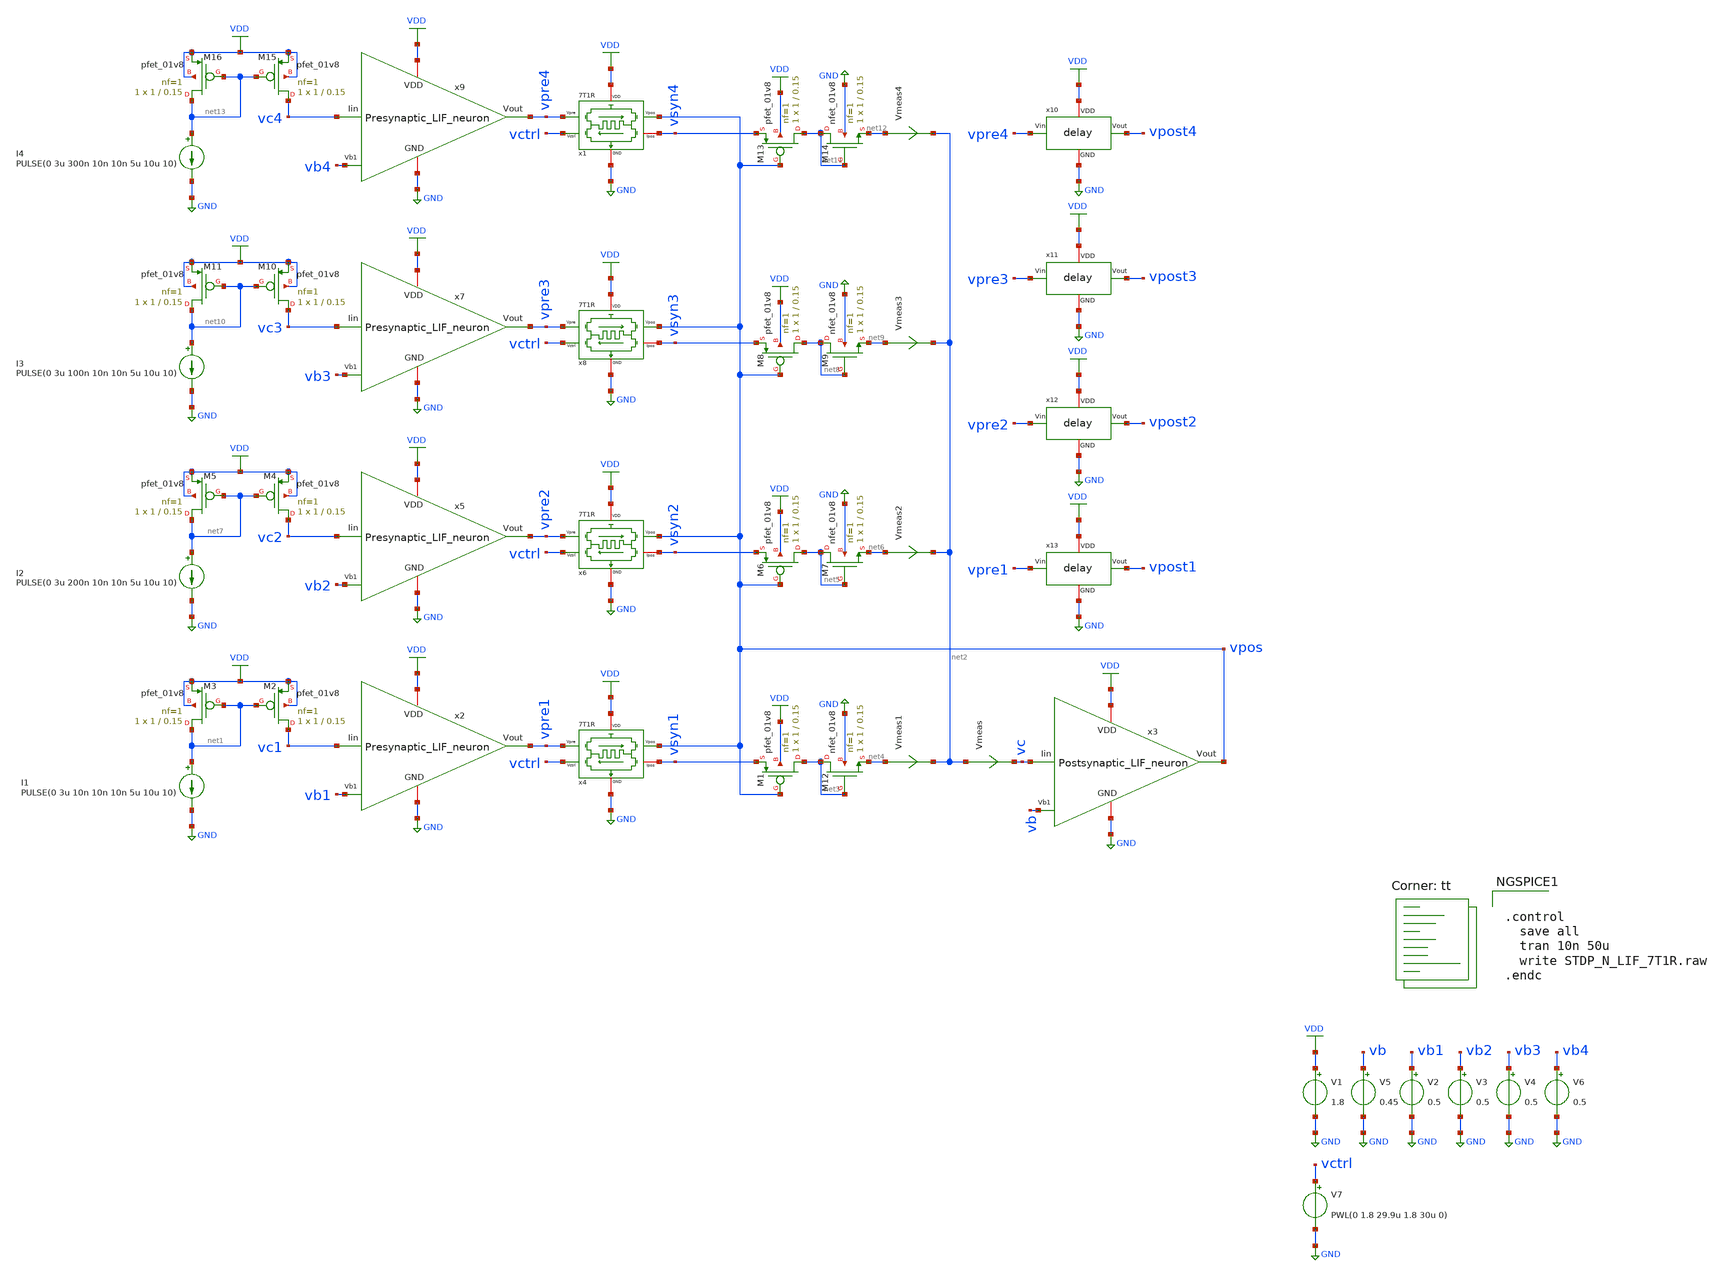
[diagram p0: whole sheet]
** sch_path: STDP/STDP_N_LIF_7T1R.sch
**.subckt STDP_N_LIF_7T1R
V1 VDD GND 1.8
V2 vb1 GND 0.5
I1 net1 GND PULSE(0 3u 10n 10n 10n 5u 10u 10)
XM2 vc1 net1 VDD VDD sky130_fd_pr__pfet_01v8 L=0.15 W=1 nf=1 ad='int((nf+1)/2) * W/nf * 0.29' as='int((nf+2)/2) * W/nf * 0.29'
+ pd='2*int((nf+1)/2) * (W/nf + 0.29)' ps='2*int((nf+2)/2) * (W/nf + 0.29)' nrd='0.29 / W' nrs='0.29 / W'
+ sa=0 sb=0 sd=0 mult=1 m=1
XM3 net1 net1 VDD VDD sky130_fd_pr__pfet_01v8 L=0.15 W=1 nf=1 ad='int((nf+1)/2) * W/nf * 0.29' as='int((nf+2)/2) * W/nf * 0.29'
+ pd='2*int((nf+1)/2) * (W/nf + 0.29)' ps='2*int((nf+2)/2) * (W/nf + 0.29)' nrd='0.29 / W' nrs='0.29 / W'
+ sa=0 sb=0 sd=0 mult=1 m=1
XM1 net3 vpos vsyn1 VDD sky130_fd_pr__pfet_01v8 L=0.15 W=1 nf=1 ad='int((nf+1)/2) * W/nf * 0.29' as='int((nf+2)/2) * W/nf * 0.29'
+ pd='2*int((nf+1)/2) * (W/nf + 0.29)' ps='2*int((nf+2)/2) * (W/nf + 0.29)' nrd='0.29 / W' nrs='0.29 / W'
+ sa=0 sb=0 sd=0 mult=1 m=1
Vmeas1 net4 net2 0
.save i(vmeas1)
V3 vb2 GND 0.5
V4 vb3 GND 0.5
Vmeas net2 vc 0
.save i(vmeas)
x2 VDD vpre1 vb1 GND vc1 Presynaptic_LIF_neuron
x3 vc VDD vpos vb GND Postsynaptic_LIF_neuron
V5 vb GND 0.45
XM12 net3 net3 net4 GND sky130_fd_pr__nfet_01v8 L=0.15 W=1 nf=1 ad='int((nf+1)/2) * W/nf * 0.29' as='int((nf+2)/2) * W/nf * 0.29'
+ pd='2*int((nf+1)/2) * (W/nf + 0.29)' ps='2*int((nf+2)/2) * (W/nf + 0.29)' nrd='0.29 / W' nrs='0.29 / W'
+ sa=0 sb=0 sd=0 mult=1 m=1
XM6 net5 vpos vsyn2 VDD sky130_fd_pr__pfet_01v8 L=0.15 W=1 nf=1 ad='int((nf+1)/2) * W/nf * 0.29' as='int((nf+2)/2) * W/nf * 0.29'
+ pd='2*int((nf+1)/2) * (W/nf + 0.29)' ps='2*int((nf+2)/2) * (W/nf + 0.29)' nrd='0.29 / W' nrs='0.29 / W'
+ sa=0 sb=0 sd=0 mult=1 m=1
Vmeas2 net6 net2 0
.save i(vmeas2)
x5 VDD vpre2 vb2 GND vc2 Presynaptic_LIF_neuron
XM7 net5 net5 net6 GND sky130_fd_pr__nfet_01v8 L=0.15 W=1 nf=1 ad='int((nf+1)/2) * W/nf * 0.29' as='int((nf+2)/2) * W/nf * 0.29'
+ pd='2*int((nf+1)/2) * (W/nf + 0.29)' ps='2*int((nf+2)/2) * (W/nf + 0.29)' nrd='0.29 / W' nrs='0.29 / W'
+ sa=0 sb=0 sd=0 mult=1 m=1
I2 net7 GND PULSE(0 3u 200n 10n 10n 5u 10u 10)
XM4 vc2 net7 VDD VDD sky130_fd_pr__pfet_01v8 L=0.15 W=1 nf=1 ad='int((nf+1)/2) * W/nf * 0.29' as='int((nf+2)/2) * W/nf * 0.29'
+ pd='2*int((nf+1)/2) * (W/nf + 0.29)' ps='2*int((nf+2)/2) * (W/nf + 0.29)' nrd='0.29 / W' nrs='0.29 / W'
+ sa=0 sb=0 sd=0 mult=1 m=1
XM5 net7 net7 VDD VDD sky130_fd_pr__pfet_01v8 L=0.15 W=1 nf=1 ad='int((nf+1)/2) * W/nf * 0.29' as='int((nf+2)/2) * W/nf * 0.29'
+ pd='2*int((nf+1)/2) * (W/nf + 0.29)' ps='2*int((nf+2)/2) * (W/nf + 0.29)' nrd='0.29 / W' nrs='0.29 / W'
+ sa=0 sb=0 sd=0 mult=1 m=1
XM8 net8 vpos vsyn3 VDD sky130_fd_pr__pfet_01v8 L=0.15 W=1 nf=1 ad='int((nf+1)/2) * W/nf * 0.29' as='int((nf+2)/2) * W/nf * 0.29'
+ pd='2*int((nf+1)/2) * (W/nf + 0.29)' ps='2*int((nf+2)/2) * (W/nf + 0.29)' nrd='0.29 / W' nrs='0.29 / W'
+ sa=0 sb=0 sd=0 mult=1 m=1
Vmeas3 net9 net2 0
.save i(vmeas3)
x7 VDD vpre3 vb3 GND vc3 Presynaptic_LIF_neuron
XM9 net8 net8 net9 GND sky130_fd_pr__nfet_01v8 L=0.15 W=1 nf=1 ad='int((nf+1)/2) * W/nf * 0.29' as='int((nf+2)/2) * W/nf * 0.29'
+ pd='2*int((nf+1)/2) * (W/nf + 0.29)' ps='2*int((nf+2)/2) * (W/nf + 0.29)' nrd='0.29 / W' nrs='0.29 / W'
+ sa=0 sb=0 sd=0 mult=1 m=1
I3 net10 GND PULSE(0 3u 100n 10n 10n 5u 10u 10)
XM10 vc3 net10 VDD VDD sky130_fd_pr__pfet_01v8 L=0.15 W=1 nf=1 ad='int((nf+1)/2) * W/nf * 0.29' as='int((nf+2)/2) * W/nf * 0.29'
+ pd='2*int((nf+1)/2) * (W/nf + 0.29)' ps='2*int((nf+2)/2) * (W/nf + 0.29)' nrd='0.29 / W' nrs='0.29 / W'
+ sa=0 sb=0 sd=0 mult=1 m=1
XM11 net10 net10 VDD VDD sky130_fd_pr__pfet_01v8 L=0.15 W=1 nf=1 ad='int((nf+1)/2) * W/nf * 0.29' as='int((nf+2)/2) * W/nf * 0.29'
+ pd='2*int((nf+1)/2) * (W/nf + 0.29)' ps='2*int((nf+2)/2) * (W/nf + 0.29)' nrd='0.29 / W' nrs='0.29 / W'
+ sa=0 sb=0 sd=0 mult=1 m=1
XM13 net11 vpos vsyn4 VDD sky130_fd_pr__pfet_01v8 L=0.15 W=1 nf=1 ad='int((nf+1)/2) * W/nf * 0.29' as='int((nf+2)/2) * W/nf * 0.29'
+ pd='2*int((nf+1)/2) * (W/nf + 0.29)' ps='2*int((nf+2)/2) * (W/nf + 0.29)' nrd='0.29 / W' nrs='0.29 / W'
+ sa=0 sb=0 sd=0 mult=1 m=1
Vmeas4 net12 net2 0
.save i(vmeas4)
x9 VDD vpre4 vb4 GND vc4 Presynaptic_LIF_neuron
XM14 net11 net11 net12 GND sky130_fd_pr__nfet_01v8 L=0.15 W=1 nf=1 ad='int((nf+1)/2) * W/nf * 0.29' as='int((nf+2)/2) * W/nf * 0.29'
+ pd='2*int((nf+1)/2) * (W/nf + 0.29)' ps='2*int((nf+2)/2) * (W/nf + 0.29)' nrd='0.29 / W' nrs='0.29 / W'
+ sa=0 sb=0 sd=0 mult=1 m=1
I4 net13 GND PULSE(0 3u 300n 10n 10n 5u 10u 10)
XM15 vc4 net13 VDD VDD sky130_fd_pr__pfet_01v8 L=0.15 W=1 nf=1 ad='int((nf+1)/2) * W/nf * 0.29' as='int((nf+2)/2) * W/nf * 0.29'
+ pd='2*int((nf+1)/2) * (W/nf + 0.29)' ps='2*int((nf+2)/2) * (W/nf + 0.29)' nrd='0.29 / W' nrs='0.29 / W'
+ sa=0 sb=0 sd=0 mult=1 m=1
XM16 net13 net13 VDD VDD sky130_fd_pr__pfet_01v8 L=0.15 W=1 nf=1 ad='int((nf+1)/2) * W/nf * 0.29' as='int((nf+2)/2) * W/nf * 0.29'
+ pd='2*int((nf+1)/2) * (W/nf + 0.29)' ps='2*int((nf+2)/2) * (W/nf + 0.29)' nrd='0.29 / W' nrs='0.29 / W'
+ sa=0 sb=0 sd=0 mult=1 m=1
V6 vb4 GND 0.5
x10 VDD vpre4 vpost4 GND delay
x11 VDD vpre3 vpost3 GND delay
x12 VDD vpre2 vpost2 GND delay
x13 VDD vpre1 vpost1 GND delay
V7 vctrl GND PWL(0 1.8 29.9u 1.8 30u 0)
x1 vctrl VDD vsyn4 vpre4 vpos GND 7T1R
x4 vctrl VDD vsyn1 vpre1 vpos GND 7T1R
x6 vctrl VDD vsyn2 vpre2 vpos GND 7T1R
x8 vctrl VDD vsyn3 vpre3 vpos GND 7T1R
**** begin user architecture code
.lib $::SKYWATER_MODELS/sky130.lib.spice tt

** opencircuitdesign pdks install
.inc $::SKYWATER_MODELS/rram_v0.spice



.control
  save all
  tran 10n 50u
  write STDP_N_LIF_7T1R.raw
.endc


**** end user architecture code
**.ends

* expanding   symbol:
*+  /home/ricardo/RATT_repos/Proyectos_xschem/LIF_neuron/Presynaptic_LIF_neuron.sym # of pins=5
** sym_path: LIF_neuron/Presynaptic_LIF_neuron.sym
** sch_path: LIF_neuron/Presynaptic_LIF_neuron.sch
.subckt Presynaptic_LIF_neuron VDD Vout Vb1 GND Iin
*.iopin GND
*.ipin Vb1
*.iopin VDD
*.opin Vout
*.ipin Iin
XM13 net2 Vb1 GND GND sky130_fd_pr__nfet_01v8 L=0.5 W=5 nf=1 ad='int((nf+1)/2) * W/nf * 0.29' as='int((nf+2)/2) * W/nf * 0.29'
+ pd='2*int((nf+1)/2) * (W/nf + 0.29)' ps='2*int((nf+2)/2) * (W/nf + 0.29)' nrd='0.29 / W' nrs='0.29 / W'
+ sa=0 sb=0 sd=0 mult=1 m=1
XM12 Crefr net1 net2 GND sky130_fd_pr__nfet_01v8 L=1 W=1 nf=1 ad='int((nf+1)/2) * W/nf * 0.29' as='int((nf+2)/2) * W/nf * 0.29'
+ pd='2*int((nf+1)/2) * (W/nf + 0.29)' ps='2*int((nf+2)/2) * (W/nf + 0.29)' nrd='0.29 / W' nrs='0.29 / W'
+ sa=0 sb=0 sd=0 mult=1 m=1
XM11 Crefr net1 VDD VDD sky130_fd_pr__pfet_01v8 L=1 W=1 nf=1 ad='int((nf+1)/2) * W/nf * 0.29' as='int((nf+2)/2) * W/nf * 0.29'
+ pd='2*int((nf+1)/2) * (W/nf + 0.29)' ps='2*int((nf+2)/2) * (W/nf + 0.29)' nrd='0.29 / W' nrs='0.29 / W'
+ sa=0 sb=0 sd=0 mult=1 m=1
XCrefr Crefr GND sky130_fd_pr__cap_mim_m3_1 W=10 L=1 MF=1 m=1
XM14 Iin Crefr GND GND sky130_fd_pr__nfet_01v8 L=6 W=0.45 nf=1 ad='int((nf+1)/2) * W/nf * 0.29' as='int((nf+2)/2) * W/nf * 0.29'
+ pd='2*int((nf+1)/2) * (W/nf + 0.29)' ps='2*int((nf+2)/2) * (W/nf + 0.29)' nrd='0.29 / W' nrs='0.29 / W'
+ sa=0 sb=0 sd=0 mult=1 m=1
XCm Iin GND sky130_fd_pr__cap_mim_m3_1 W=10 L=1 MF=30 m=30
XM6 net3 Vout GND GND sky130_fd_pr__nfet_01v8 L=0.5 W=1 nf=1 ad='int((nf+1)/2) * W/nf * 0.29' as='int((nf+2)/2) * W/nf * 0.29'
+ pd='2*int((nf+1)/2) * (W/nf + 0.29)' ps='2*int((nf+2)/2) * (W/nf + 0.29)' nrd='0.29 / W' nrs='0.29 / W'
+ sa=0 sb=0 sd=0 mult=1 m=1
XM7 net1 Iin net3 GND sky130_fd_pr__nfet_01v8 L=1 W=1 nf=1 ad='int((nf+1)/2) * W/nf * 0.29' as='int((nf+2)/2) * W/nf * 0.29'
+ pd='2*int((nf+1)/2) * (W/nf + 0.29)' ps='2*int((nf+2)/2) * (W/nf + 0.29)' nrd='0.29 / W' nrs='0.29 / W'
+ sa=0 sb=0 sd=0 mult=1 m=1
XM8 net1 Iin VDD VDD sky130_fd_pr__pfet_01v8 L=1 W=1 nf=1 ad='int((nf+1)/2) * W/nf * 0.29' as='int((nf+2)/2) * W/nf * 0.29'
+ pd='2*int((nf+1)/2) * (W/nf + 0.29)' ps='2*int((nf+2)/2) * (W/nf + 0.29)' nrd='0.29 / W' nrs='0.29 / W'
+ sa=0 sb=0 sd=0 mult=1 m=1
XM9 Vout net1 net3 GND sky130_fd_pr__nfet_01v8 L=1 W=1 nf=1 ad='int((nf+1)/2) * W/nf * 0.29' as='int((nf+2)/2) * W/nf * 0.29'
+ pd='2*int((nf+1)/2) * (W/nf + 0.29)' ps='2*int((nf+2)/2) * (W/nf + 0.29)' nrd='0.29 / W' nrs='0.29 / W'
+ sa=0 sb=0 sd=0 mult=1 m=1
XM10 Vout net1 VDD VDD sky130_fd_pr__pfet_01v8 L=1 W=5 nf=1 ad='int((nf+1)/2) * W/nf * 0.29' as='int((nf+2)/2) * W/nf * 0.29'
+ pd='2*int((nf+1)/2) * (W/nf + 0.29)' ps='2*int((nf+2)/2) * (W/nf + 0.29)' nrd='0.29 / W' nrs='0.29 / W'
+ sa=0 sb=0 sd=0 mult=1 m=1
.ends


* expanding   symbol:
*+  /home/ricardo/RATT_repos/Proyectos_xschem/LIF_neuron/Postsynaptic_LIF_neuron.sym # of pins=5
** sym_path: LIF_neuron/Postsynaptic_LIF_neuron.sym
** sch_path: LIF_neuron/Postsynaptic_LIF_neuron.sch
.subckt Postsynaptic_LIF_neuron Iin VDD Vout Vb1 GND
*.iopin GND
*.ipin Vb1
*.iopin VDD
*.opin Vout
*.ipin Iin
XM13 net2 Vb1 GND GND sky130_fd_pr__nfet_01v8 L=0.5 W=5 nf=1 ad='int((nf+1)/2) * W/nf * 0.29' as='int((nf+2)/2) * W/nf * 0.29'
+ pd='2*int((nf+1)/2) * (W/nf + 0.29)' ps='2*int((nf+2)/2) * (W/nf + 0.29)' nrd='0.29 / W' nrs='0.29 / W'
+ sa=0 sb=0 sd=0 mult=1 m=1
XM12 Crefr net1 net2 GND sky130_fd_pr__nfet_01v8 L=1 W=1 nf=1 ad='int((nf+1)/2) * W/nf * 0.29' as='int((nf+2)/2) * W/nf * 0.29'
+ pd='2*int((nf+1)/2) * (W/nf + 0.29)' ps='2*int((nf+2)/2) * (W/nf + 0.29)' nrd='0.29 / W' nrs='0.29 / W'
+ sa=0 sb=0 sd=0 mult=1 m=1
XM11 Crefr net1 VDD VDD sky130_fd_pr__pfet_01v8 L=1 W=1 nf=1 ad='int((nf+1)/2) * W/nf * 0.29' as='int((nf+2)/2) * W/nf * 0.29'
+ pd='2*int((nf+1)/2) * (W/nf + 0.29)' ps='2*int((nf+2)/2) * (W/nf + 0.29)' nrd='0.29 / W' nrs='0.29 / W'
+ sa=0 sb=0 sd=0 mult=1 m=1
XC1 Crefr GND sky130_fd_pr__cap_mim_m3_1 W=21 L=1 MF=1 m=1
XM14 Iin Crefr GND GND sky130_fd_pr__nfet_01v8 L=40 W=1 nf=1 ad='int((nf+1)/2) * W/nf * 0.29' as='int((nf+2)/2) * W/nf * 0.29'
+ pd='2*int((nf+1)/2) * (W/nf + 0.29)' ps='2*int((nf+2)/2) * (W/nf + 0.29)' nrd='0.29 / W' nrs='0.29 / W'
+ sa=0 sb=0 sd=0 mult=1 m=1
XC2 Iin GND sky130_fd_pr__cap_mim_m3_1 W=20 L=1 MF=50 m=50
XM6 net3 Vout GND GND sky130_fd_pr__nfet_01v8 L=0.5 W=1 nf=1 ad='int((nf+1)/2) * W/nf * 0.29' as='int((nf+2)/2) * W/nf * 0.29'
+ pd='2*int((nf+1)/2) * (W/nf + 0.29)' ps='2*int((nf+2)/2) * (W/nf + 0.29)' nrd='0.29 / W' nrs='0.29 / W'
+ sa=0 sb=0 sd=0 mult=1 m=1
XM7 net1 Iin net3 GND sky130_fd_pr__nfet_01v8 L=1 W=1 nf=1 ad='int((nf+1)/2) * W/nf * 0.29' as='int((nf+2)/2) * W/nf * 0.29'
+ pd='2*int((nf+1)/2) * (W/nf + 0.29)' ps='2*int((nf+2)/2) * (W/nf + 0.29)' nrd='0.29 / W' nrs='0.29 / W'
+ sa=0 sb=0 sd=0 mult=1 m=1
XM8 net1 Iin VDD VDD sky130_fd_pr__pfet_01v8 L=1 W=1 nf=1 ad='int((nf+1)/2) * W/nf * 0.29' as='int((nf+2)/2) * W/nf * 0.29'
+ pd='2*int((nf+1)/2) * (W/nf + 0.29)' ps='2*int((nf+2)/2) * (W/nf + 0.29)' nrd='0.29 / W' nrs='0.29 / W'
+ sa=0 sb=0 sd=0 mult=1 m=1
XM9 Vout net1 net3 GND sky130_fd_pr__nfet_01v8 L=1 W=1 nf=1 ad='int((nf+1)/2) * W/nf * 0.29' as='int((nf+2)/2) * W/nf * 0.29'
+ pd='2*int((nf+1)/2) * (W/nf + 0.29)' ps='2*int((nf+2)/2) * (W/nf + 0.29)' nrd='0.29 / W' nrs='0.29 / W'
+ sa=0 sb=0 sd=0 mult=1 m=1
XM10 Vout net1 VDD VDD sky130_fd_pr__pfet_01v8 L=1 W=5 nf=1 ad='int((nf+1)/2) * W/nf * 0.29' as='int((nf+2)/2) * W/nf * 0.29'
+ pd='2*int((nf+1)/2) * (W/nf + 0.29)' ps='2*int((nf+2)/2) * (W/nf + 0.29)' nrd='0.29 / W' nrs='0.29 / W'
+ sa=0 sb=0 sd=0 mult=1 m=1
.ends


* expanding   symbol:  /home/ricardo/RATT_repos/Proyectos_xschem/delay/delay.sym # of pins=4
** sym_path: delay/delay.sym
** sch_path: delay/delay.sch
.subckt delay VDD Vin Vout GND
*.ipin Vin
*.opin Vout
*.iopin VDD
*.iopin GND
XM1 net1 Vin VDD VDD sky130_fd_pr__pfet_01v8 L=6 W=0.45 nf=1 ad='int((nf+1)/2) * W/nf * 0.29' as='int((nf+2)/2) * W/nf * 0.29'
+ pd='2*int((nf+1)/2) * (W/nf + 0.29)' ps='2*int((nf+2)/2) * (W/nf + 0.29)' nrd='0.29 / W' nrs='0.29 / W'
+ sa=0 sb=0 sd=0 mult=1 m=1
XM2 net1 Vin GND GND sky130_fd_pr__nfet_01v8 L=6 W=0.45 nf=1 ad='int((nf+1)/2) * W/nf * 0.29' as='int((nf+2)/2) * W/nf * 0.29'
+ pd='2*int((nf+1)/2) * (W/nf + 0.29)' ps='2*int((nf+2)/2) * (W/nf + 0.29)' nrd='0.29 / W' nrs='0.29 / W'
+ sa=0 sb=0 sd=0 mult=1 m=1
XM3 net2 net1 VDD VDD sky130_fd_pr__pfet_01v8 L=6 W=0.45 nf=1 ad='int((nf+1)/2) * W/nf * 0.29' as='int((nf+2)/2) * W/nf * 0.29'
+ pd='2*int((nf+1)/2) * (W/nf + 0.29)' ps='2*int((nf+2)/2) * (W/nf + 0.29)' nrd='0.29 / W' nrs='0.29 / W'
+ sa=0 sb=0 sd=0 mult=1 m=1
XM4 net2 net1 GND GND sky130_fd_pr__nfet_01v8 L=6 W=0.45 nf=1 ad='int((nf+1)/2) * W/nf * 0.29' as='int((nf+2)/2) * W/nf * 0.29'
+ pd='2*int((nf+1)/2) * (W/nf + 0.29)' ps='2*int((nf+2)/2) * (W/nf + 0.29)' nrd='0.29 / W' nrs='0.29 / W'
+ sa=0 sb=0 sd=0 mult=1 m=1
XM5 net3 net2 VDD VDD sky130_fd_pr__pfet_01v8 L=6 W=0.45 nf=1 ad='int((nf+1)/2) * W/nf * 0.29' as='int((nf+2)/2) * W/nf * 0.29'
+ pd='2*int((nf+1)/2) * (W/nf + 0.29)' ps='2*int((nf+2)/2) * (W/nf + 0.29)' nrd='0.29 / W' nrs='0.29 / W'
+ sa=0 sb=0 sd=0 mult=1 m=1
XM6 net3 net2 GND GND sky130_fd_pr__nfet_01v8 L=6 W=0.45 nf=1 ad='int((nf+1)/2) * W/nf * 0.29' as='int((nf+2)/2) * W/nf * 0.29'
+ pd='2*int((nf+1)/2) * (W/nf + 0.29)' ps='2*int((nf+2)/2) * (W/nf + 0.29)' nrd='0.29 / W' nrs='0.29 / W'
+ sa=0 sb=0 sd=0 mult=1 m=1
XM7 Vout net3 VDD VDD sky130_fd_pr__pfet_01v8 L=6 W=0.45 nf=1 ad='int((nf+1)/2) * W/nf * 0.29' as='int((nf+2)/2) * W/nf * 0.29'
+ pd='2*int((nf+1)/2) * (W/nf + 0.29)' ps='2*int((nf+2)/2) * (W/nf + 0.29)' nrd='0.29 / W' nrs='0.29 / W'
+ sa=0 sb=0 sd=0 mult=1 m=1
XM8 Vout net3 GND GND sky130_fd_pr__nfet_01v8 L=6 W=0.45 nf=1 ad='int((nf+1)/2) * W/nf * 0.29' as='int((nf+2)/2) * W/nf * 0.29'
+ pd='2*int((nf+1)/2) * (W/nf + 0.29)' ps='2*int((nf+2)/2) * (W/nf + 0.29)' nrd='0.29 / W' nrs='0.29 / W'
+ sa=0 sb=0 sd=0 mult=1 m=1
.ends


* expanding   symbol:  /home/ricardo/RATT_repos/Proyectos_xschem/synapse/7T1R.sym # of pins=6
** sym_path: synapse/7T1R.sym
** sch_path: synapse/7T1R.sch
.subckt 7T1R Vctrl VDD Ipos Vpre Vpos GND
*.ipin Vpre
*.ipin Vpos
*.iopin GND
*.iopin Ipos
*.iopin VDD
*.ipin Vctrl
XM1 vipre Vpre BE GND sky130_fd_pr__nfet_01v8 L=0.15 W=1 nf=1 ad='int((nf+1)/2) * W/nf * 0.29' as='int((nf+2)/2) * W/nf * 0.29'
+ pd='2*int((nf+1)/2) * (W/nf + 0.29)' ps='2*int((nf+2)/2) * (W/nf + 0.29)' nrd='0.29 / W' nrs='0.29 / W'
+ sa=0 sb=0 sd=0 mult=1 m=1
XR1 TE BE rram_v0
XM3 vipre Vpos TE GND sky130_fd_pr__nfet_01v8 L=0.15 W=20 nf=1 ad='int((nf+1)/2) * W/nf * 0.29' as='int((nf+2)/2) * W/nf * 0.29'
+ pd='2*int((nf+1)/2) * (W/nf + 0.29)' ps='2*int((nf+2)/2) * (W/nf + 0.29)' nrd='0.29 / W' nrs='0.29 / W'
+ sa=0 sb=0 sd=0 mult=1 m=1
XM6 Ipos vipre net1 net1 sky130_fd_pr__pfet_01v8 L=0.15 W=20 nf=1 ad='int((nf+1)/2) * W/nf * 0.29' as='int((nf+2)/2) * W/nf * 0.29'
+ pd='2*int((nf+1)/2) * (W/nf + 0.29)' ps='2*int((nf+2)/2) * (W/nf + 0.29)' nrd='0.29 / W' nrs='0.29 / W'
+ sa=0 sb=0 sd=0 mult=1 m=1
XM5 vipre vipre net1 net1 sky130_fd_pr__pfet_01v8 L=0.15 W=20 nf=1 ad='int((nf+1)/2) * W/nf * 0.29' as='int((nf+2)/2) * W/nf * 0.29'
+ pd='2*int((nf+1)/2) * (W/nf + 0.29)' ps='2*int((nf+2)/2) * (W/nf + 0.29)' nrd='0.29 / W' nrs='0.29 / W'
+ sa=0 sb=0 sd=0 mult=1 m=1
XM2 BE Vpos GND GND sky130_fd_pr__nfet_01v8 L=0.15 W=20 nf=1 ad='int((nf+1)/2) * W/nf * 0.29' as='int((nf+2)/2) * W/nf * 0.29'
+ pd='2*int((nf+1)/2) * (W/nf + 0.29)' ps='2*int((nf+2)/2) * (W/nf + 0.29)' nrd='0.29 / W' nrs='0.29 / W'
+ sa=0 sb=0 sd=0 mult=1 m=1
XM4 TE Vpre GND GND sky130_fd_pr__nfet_01v8 L=0.15 W=1 nf=1 ad='int((nf+1)/2) * W/nf * 0.29' as='int((nf+2)/2) * W/nf * 0.29'
+ pd='2*int((nf+1)/2) * (W/nf + 0.29)' ps='2*int((nf+2)/2) * (W/nf + 0.29)' nrd='0.29 / W' nrs='0.29 / W'
+ sa=0 sb=0 sd=0 mult=1 m=1
XM7 VDD Vctrl net1 GND sky130_fd_pr__nfet_01v8 L=0.15 W=20 nf=1 ad='int((nf+1)/2) * W/nf * 0.29' as='int((nf+2)/2) * W/nf * 0.29'
+ pd='2*int((nf+1)/2) * (W/nf + 0.29)' ps='2*int((nf+2)/2) * (W/nf + 0.29)' nrd='0.29 / W' nrs='0.29 / W'
+ sa=0 sb=0 sd=0 mult=1 m=1
.ends

.GLOBAL GND
.GLOBAL VDD
.end
